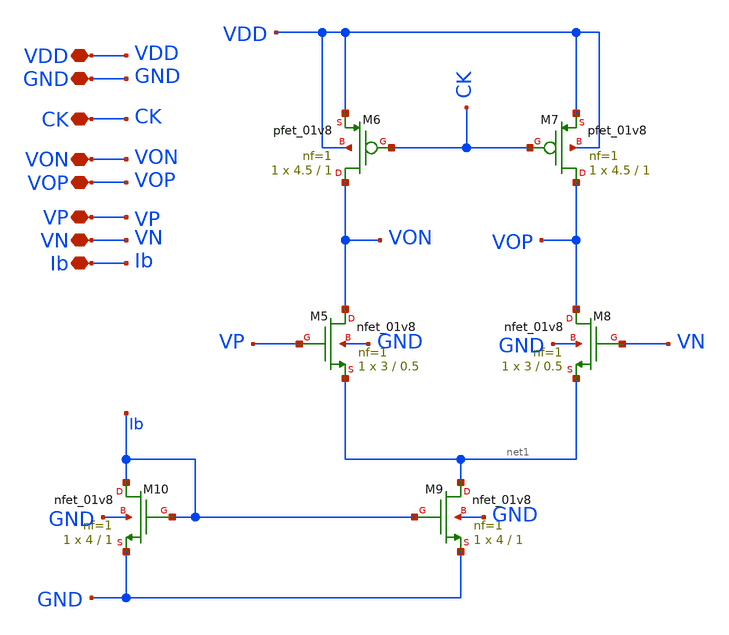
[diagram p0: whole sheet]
** sch_path: xschem/comparator/preamp.sch
**.subckt preamp VDD GND CK VON VOP VP VN Ib
*.iopin VDD
*.iopin GND
*.iopin CK
*.iopin VON
*.iopin VOP
*.iopin VP
*.iopin VN
*.iopin Ib
XM5 VON VP net1 GND sky130_fd_pr__nfet_01v8 L=0.5 W=3 nf=1 ad='int((1 + 1)/2) * 3 / 1 * 0.29' as='int((1 + 2)/2) * 3 / 1 * 0.29'
+ pd='2*int((1 + 1)/2) * (3 / 1 + 0.29)' ps='2*int((1 + 2)/2) * (3 / 1 + 0.29)' nrd='0.29 / 3 ' nrs='0.29 / 3 '
+ sa=0 sb=0 sd=0 mult=1 m=1
XM6 VON CK VDD VDD sky130_fd_pr__pfet_01v8 L=1 W=4.5 nf=1 ad='int((nf+1)/2) * W/nf * 0.29' as='int((nf+2)/2) * W/nf * 0.29'
+ pd='2*int((nf+1)/2) * (W/nf + 0.29)' ps='2*int((nf+2)/2) * (W/nf + 0.29)' nrd='0.29 / W' nrs='0.29 / W'
+ sa=0 sb=0 sd=0 mult=1 m=1
XM7 VOP CK VDD VDD sky130_fd_pr__pfet_01v8 L=1 W=4.5 nf=1 ad='int((nf+1)/2) * W/nf * 0.29' as='int((nf+2)/2) * W/nf * 0.29'
+ pd='2*int((nf+1)/2) * (W/nf + 0.29)' ps='2*int((nf+2)/2) * (W/nf + 0.29)' nrd='0.29 / W' nrs='0.29 / W'
+ sa=0 sb=0 sd=0 mult=1 m=1
XM8 VOP VN net1 GND sky130_fd_pr__nfet_01v8 L=0.5 W=3 nf=1 ad='int((1 + 1)/2) * 3 / 1 * 0.29' as='int((1 + 2)/2) * 3 / 1 * 0.29'
+ pd='2*int((1 + 1)/2) * (3 / 1 + 0.29)' ps='2*int((1 + 2)/2) * (3 / 1 + 0.29)' nrd='0.29 / 3 ' nrs='0.29 / 3 '
+ sa=0 sb=0 sd=0 mult=1 m=1
XM9 net1 Ib GND GND sky130_fd_pr__nfet_01v8 L=1 W=4 nf=1 ad='int((1 + 1)/2) * 4 / 1 * 0.29' as='int((1 + 2)/2) * 4 / 1 * 0.29'
+ pd='2*int((1 + 1)/2) * (4 / 1 + 0.29)' ps='2*int((1 + 2)/2) * (4 / 1 + 0.29)' nrd='0.29 / 4 ' nrs='0.29 / 4 '
+ sa=0 sb=0 sd=0 mult=1 m=1
XM10 Ib Ib GND GND sky130_fd_pr__nfet_01v8 L=1 W=4 nf=1 ad='int((1 + 1)/2) * 4 / 1 * 0.29' as='int((1 + 2)/2) * 4 / 1 * 0.29'
+ pd='2*int((1 + 1)/2) * (4 / 1 + 0.29)' ps='2*int((1 + 2)/2) * (4 / 1 + 0.29)' nrd='0.29 / 4 ' nrs='0.29 / 4 '
+ sa=0 sb=0 sd=0 mult=1 m=1
**.ends
.end
